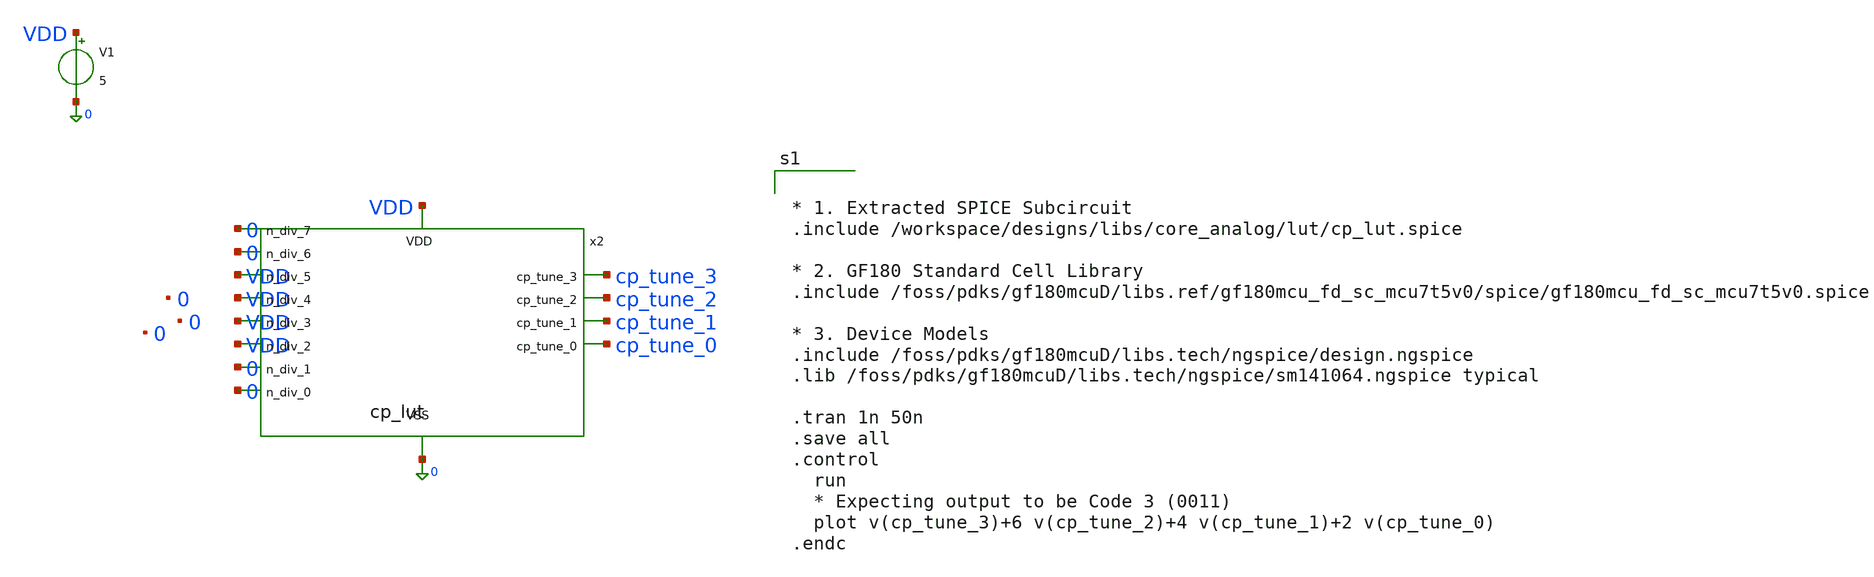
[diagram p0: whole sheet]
** sch_path: designs/libs/tb_analog/tb_lut/tb_cp_lut.sch
**.subckt tb_cp_lut
V1 VDD 0 5
x2 VDD 0 cp_tune_0 cp_tune_1 cp_tune_2 cp_tune_3 0 0 VDD VDD VDD VDD 0 0 cp_lut
**** begin user architecture code


* 1. Extracted SPICE Subcircuit
.include /workspace/designs/libs/core_analog/lut/cp_lut.spice

* 2. GF180 Standard Cell Library
.include /foss/pdks/gf180mcuD/libs.ref/gf180mcu_fd_sc_mcu7t5v0/spice/gf180mcu_fd_sc_mcu7t5v0.spice

* 3. Device Models
.include /foss/pdks/gf180mcuD/libs.tech/ngspice/design.ngspice
.lib /foss/pdks/gf180mcuD/libs.tech/ngspice/sm141064.ngspice typical

.tran 1n 50n
.save all
.control
  run
  * Expecting output to be Code 3 (0011)
  plot v(cp_tune_3)+6 v(cp_tune_2)+4 v(cp_tune_1)+2 v(cp_tune_0)
.endc

**** end user architecture code
**.ends
.end
